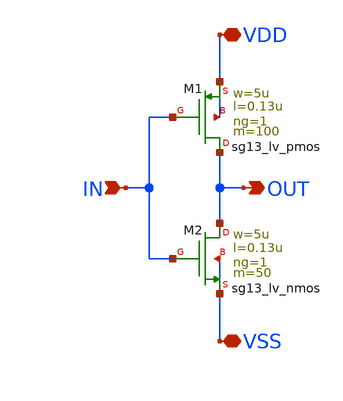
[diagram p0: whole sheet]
** sch_path: SSDOR_1.2V_v2/components/trans_gate/tg_inverter.sch
**.subckt tg_inverter VSS VDD IN OUT
*.iopin VSS
*.iopin VDD
*.ipin IN
*.opin OUT
XM1 OUT IN VDD VDD sg13_lv_pmos w=5u l=0.13u ng=1 m=100 mm_ok=1
XM2 OUT IN VSS VSS sg13_lv_nmos w=5u l=0.13u ng=1 m=50 mm_ok=1
**.ends
.end
